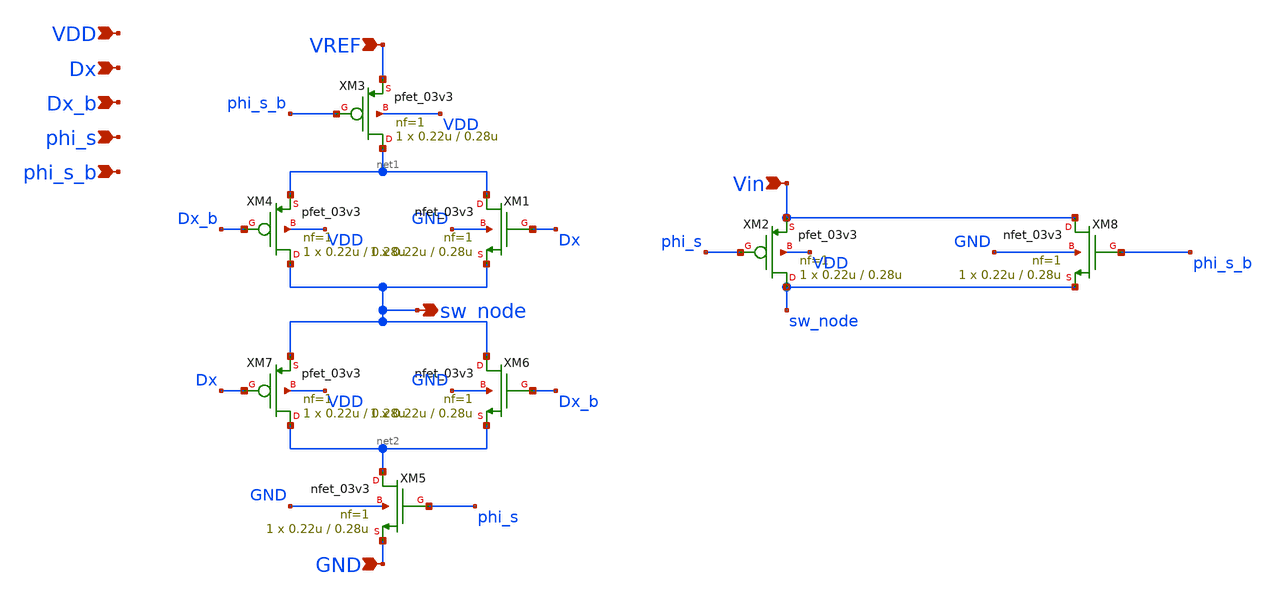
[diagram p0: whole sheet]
** sch_path: analog/blocks/cdac/transistors2.sch
**.subckt transistors2 Vin VREF sw_node GND Dx Dx_b phi_s VDD phi_s_b
*.ipin Vin
*.ipin VREF
*.opin sw_node
*.ipin GND
*.ipin Dx
*.ipin Dx_b
*.ipin phi_s
*.ipin VDD
*.ipin phi_s_b
XM4 sw_node Dx_b net1 VDD pfet_03v3 L=0.28u W=0.22u nf=1 ad='int((nf+1)/2) * W/nf * 0.18u' as='int((nf+2)/2) * W/nf * 0.18u'
+ pd='2*int((nf+1)/2) * (W/nf + 0.18u)' ps='2*int((nf+2)/2) * (W/nf + 0.18u)' nrd='0.18u / W' nrs='0.18u / W'
+ sa=0 sb=0 sd=0 m=1
XM6 sw_node Dx_b net2 GND nfet_03v3 L=0.28u W=0.22u nf=1 ad='int((nf+1)/2) * W/nf * 0.18u' as='int((nf+2)/2) * W/nf * 0.18u'
+ pd='2*int((nf+1)/2) * (W/nf + 0.18u)' ps='2*int((nf+2)/2) * (W/nf + 0.18u)' nrd='0.18u / W' nrs='0.18u / W'
+ sa=0 sb=0 sd=0 m=1
XM7 net2 Dx sw_node VDD pfet_03v3 L=0.28u W=0.22u nf=1 ad='int((nf+1)/2) * W/nf * 0.18u' as='int((nf+2)/2) * W/nf * 0.18u'
+ pd='2*int((nf+1)/2) * (W/nf + 0.18u)' ps='2*int((nf+2)/2) * (W/nf + 0.18u)' nrd='0.18u / W' nrs='0.18u / W'
+ sa=0 sb=0 sd=0 m=1
XM2 sw_node phi_s Vin VDD pfet_03v3 L=0.28u W=0.22u nf=1 ad='int((nf+1)/2) * W/nf * 0.18u' as='int((nf+2)/2) * W/nf * 0.18u'
+ pd='2*int((nf+1)/2) * (W/nf + 0.18u)' ps='2*int((nf+2)/2) * (W/nf + 0.18u)' nrd='0.18u / W' nrs='0.18u / W'
+ sa=0 sb=0 sd=0 m=1
XM1 net1 Dx sw_node GND nfet_03v3 L=0.28u W=0.22u nf=1 ad='int((nf+1)/2) * W/nf * 0.18u' as='int((nf+2)/2) * W/nf * 0.18u'
+ pd='2*int((nf+1)/2) * (W/nf + 0.18u)' ps='2*int((nf+2)/2) * (W/nf + 0.18u)' nrd='0.18u / W' nrs='0.18u / W'
+ sa=0 sb=0 sd=0 m=1
XM3 net1 phi_s_b VREF VDD pfet_03v3 L=0.28u W=0.22u nf=1 ad='int((nf+1)/2) * W/nf * 0.18u' as='int((nf+2)/2) * W/nf * 0.18u'
+ pd='2*int((nf+1)/2) * (W/nf + 0.18u)' ps='2*int((nf+2)/2) * (W/nf + 0.18u)' nrd='0.18u / W' nrs='0.18u / W'
+ sa=0 sb=0 sd=0 m=1
XM5 net2 phi_s GND GND nfet_03v3 L=0.28u W=0.22u nf=1 ad='int((nf+1)/2) * W/nf * 0.18u' as='int((nf+2)/2) * W/nf * 0.18u'
+ pd='2*int((nf+1)/2) * (W/nf + 0.18u)' ps='2*int((nf+2)/2) * (W/nf + 0.18u)' nrd='0.18u / W' nrs='0.18u / W'
+ sa=0 sb=0 sd=0 m=1
XM8 Vin phi_s_b sw_node GND nfet_03v3 L=0.28u W=0.22u nf=1 ad='int((nf+1)/2) * W/nf * 0.18u' as='int((nf+2)/2) * W/nf * 0.18u'
+ pd='2*int((nf+1)/2) * (W/nf + 0.18u)' ps='2*int((nf+2)/2) * (W/nf + 0.18u)' nrd='0.18u / W' nrs='0.18u / W'
+ sa=0 sb=0 sd=0 m=1
**.ends
.end
